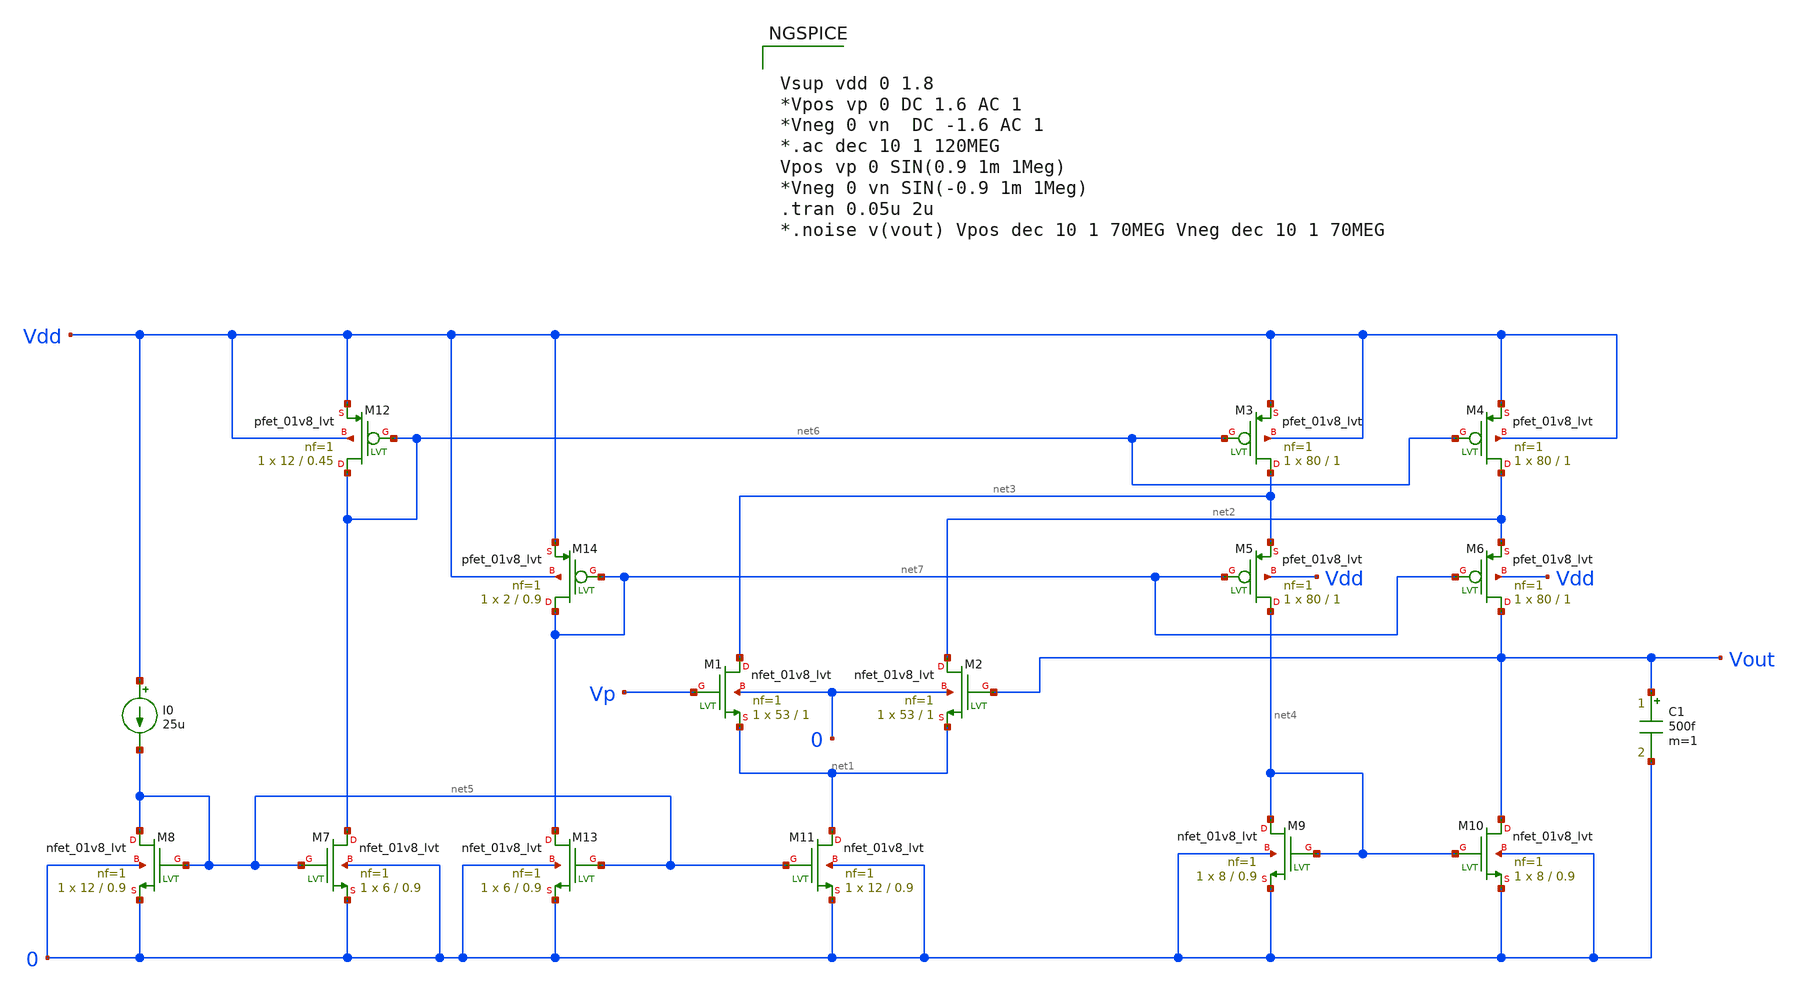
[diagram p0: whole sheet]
** sch_path: OTA/Schematic/Folded_Cascode_OTA.sch
**.subckt Folded_Cascode_OTA
XM1 net3 Vp net1 0 sky130_fd_pr__nfet_01v8_lvt L=1 W=53 nf=1 ad='int((nf+1)/2) * W/nf * 0.29' as='int((nf+2)/2) * W/nf * 0.29'
+ pd='2*int((nf+1)/2) * (W/nf + 0.29)' ps='2*int((nf+2)/2) * (W/nf + 0.29)' nrd='0.29 / W' nrs='0.29 / W'
+ sa=0 sb=0 sd=0 mult=1 m=1
XM2 net2 Vout net1 0 sky130_fd_pr__nfet_01v8_lvt L=1 W=53 nf=1 ad='int((nf+1)/2) * W/nf * 0.29' as='int((nf+2)/2) * W/nf * 0.29'
+ pd='2*int((nf+1)/2) * (W/nf + 0.29)' ps='2*int((nf+2)/2) * (W/nf + 0.29)' nrd='0.29 / W' nrs='0.29 / W'
+ sa=0 sb=0 sd=0 mult=1 m=1
XM3 net3 net6 Vdd Vdd sky130_fd_pr__pfet_01v8_lvt L=1 W=80 nf=1 ad='int((nf+1)/2) * W/nf * 0.29' as='int((nf+2)/2) * W/nf * 0.29'
+ pd='2*int((nf+1)/2) * (W/nf + 0.29)' ps='2*int((nf+2)/2) * (W/nf + 0.29)' nrd='0.29 / W' nrs='0.29 / W'
+ sa=0 sb=0 sd=0 mult=1 m=1
XM4 net2 net6 Vdd Vdd sky130_fd_pr__pfet_01v8_lvt L=1 W=80 nf=1 ad='int((nf+1)/2) * W/nf * 0.29' as='int((nf+2)/2) * W/nf * 0.29'
+ pd='2*int((nf+1)/2) * (W/nf + 0.29)' ps='2*int((nf+2)/2) * (W/nf + 0.29)' nrd='0.29 / W' nrs='0.29 / W'
+ sa=0 sb=0 sd=0 mult=1 m=1
XM5 net4 net7 net3 Vdd sky130_fd_pr__pfet_01v8_lvt L=1 W=80 nf=1 ad='int((nf+1)/2) * W/nf * 0.29' as='int((nf+2)/2) * W/nf * 0.29'
+ pd='2*int((nf+1)/2) * (W/nf + 0.29)' ps='2*int((nf+2)/2) * (W/nf + 0.29)' nrd='0.29 / W' nrs='0.29 / W'
+ sa=0 sb=0 sd=0 mult=1 m=1
XM6 Vout net7 net2 Vdd sky130_fd_pr__pfet_01v8_lvt L=1 W=80 nf=1 ad='int((nf+1)/2) * W/nf * 0.29' as='int((nf+2)/2) * W/nf * 0.29'
+ pd='2*int((nf+1)/2) * (W/nf + 0.29)' ps='2*int((nf+2)/2) * (W/nf + 0.29)' nrd='0.29 / W' nrs='0.29 / W'
+ sa=0 sb=0 sd=0 mult=1 m=1
XM9 net4 net4 0 0 sky130_fd_pr__nfet_01v8_lvt L=0.9 W=8 nf=1 ad='int((nf+1)/2) * W/nf * 0.29' as='int((nf+2)/2) * W/nf * 0.29'
+ pd='2*int((nf+1)/2) * (W/nf + 0.29)' ps='2*int((nf+2)/2) * (W/nf + 0.29)' nrd='0.29 / W' nrs='0.29 / W'
+ sa=0 sb=0 sd=0 mult=1 m=1
XM10 Vout net4 0 0 sky130_fd_pr__nfet_01v8_lvt L=0.9 W=8 nf=1 ad='int((nf+1)/2) * W/nf * 0.29' as='int((nf+2)/2) * W/nf * 0.29'
+ pd='2*int((nf+1)/2) * (W/nf + 0.29)' ps='2*int((nf+2)/2) * (W/nf + 0.29)' nrd='0.29 / W' nrs='0.29 / W'
+ sa=0 sb=0 sd=0 mult=1 m=1
XM11 net1 net5 0 0 sky130_fd_pr__nfet_01v8_lvt L=0.9 W=12 nf=1 ad='int((nf+1)/2) * W/nf * 0.29' as='int((nf+2)/2) * W/nf * 0.29'
+ pd='2*int((nf+1)/2) * (W/nf + 0.29)' ps='2*int((nf+2)/2) * (W/nf + 0.29)' nrd='0.29 / W' nrs='0.29 / W'
+ sa=0 sb=0 sd=0 mult=1 m=1
XM7 net6 net5 0 0 sky130_fd_pr__nfet_01v8_lvt L=0.9 W=6 nf=1 ad='int((nf+1)/2) * W/nf * 0.29' as='int((nf+2)/2) * W/nf * 0.29'
+ pd='2*int((nf+1)/2) * (W/nf + 0.29)' ps='2*int((nf+2)/2) * (W/nf + 0.29)' nrd='0.29 / W' nrs='0.29 / W'
+ sa=0 sb=0 sd=0 mult=1 m=1
XM8 net5 net5 0 0 sky130_fd_pr__nfet_01v8_lvt L=0.9 W=12 nf=1 ad='int((nf+1)/2) * W/nf * 0.29' as='int((nf+2)/2) * W/nf * 0.29'
+ pd='2*int((nf+1)/2) * (W/nf + 0.29)' ps='2*int((nf+2)/2) * (W/nf + 0.29)' nrd='0.29 / W' nrs='0.29 / W'
+ sa=0 sb=0 sd=0 mult=1 m=1
XM12 net6 net6 Vdd Vdd sky130_fd_pr__pfet_01v8_lvt L=0.45 W=12 nf=1 ad='int((nf+1)/2) * W/nf * 0.29'
+ as='int((nf+2)/2) * W/nf * 0.29' pd='2*int((nf+1)/2) * (W/nf + 0.29)' ps='2*int((nf+2)/2) * (W/nf + 0.29)'
+ nrd='0.29 / W' nrs='0.29 / W' sa=0 sb=0 sd=0 mult=1 m=1
XM13 net7 net5 0 0 sky130_fd_pr__nfet_01v8_lvt L=0.9 W=6 nf=1 ad='int((nf+1)/2) * W/nf * 0.29' as='int((nf+2)/2) * W/nf * 0.29'
+ pd='2*int((nf+1)/2) * (W/nf + 0.29)' ps='2*int((nf+2)/2) * (W/nf + 0.29)' nrd='0.29 / W' nrs='0.29 / W'
+ sa=0 sb=0 sd=0 mult=1 m=1
XM14 net7 net7 Vdd Vdd sky130_fd_pr__pfet_01v8_lvt L=0.9 W=2 nf=1 ad='int((nf+1)/2) * W/nf * 0.29' as='int((nf+2)/2) * W/nf * 0.29'
+ pd='2*int((nf+1)/2) * (W/nf + 0.29)' ps='2*int((nf+2)/2) * (W/nf + 0.29)' nrd='0.29 / W' nrs='0.29 / W'
+ sa=0 sb=0 sd=0 mult=1 m=1
I0 Vdd net5 25u
C1 Vout 0 500f m=1
**** begin user architecture code

.include $::SKYWATER_MODELS/cells/nfet_01v8/sky130_fd_pr__nfet_01v8__tt.corner.spice
.include $::SKYWATER_MODELS/cells/nfet_01v8_lvt/sky130_fd_pr__nfet_01v8_lvt__tt.corner.spice
.include $::SKYWATER_MODELS/cells/pfet_01v8/sky130_fd_pr__pfet_01v8__tt.corner.spice
.include $::SKYWATER_MODELS/cells/nfet_03v3_nvt/sky130_fd_pr__nfet_03v3_nvt__tt.corner.spice
.include $::SKYWATER_MODELS/cells/nfet_05v0_nvt/sky130_fd_pr__nfet_05v0_nvt__tt.corner.spice
.include $::SKYWATER_MODELS/cells/esd_nfet_01v8/sky130_fd_pr__esd_nfet_01v8__tt.corner.spice
.include $::SKYWATER_MODELS/cells/pfet_01v8_lvt/sky130_fd_pr__pfet_01v8_lvt__tt.corner.spice
.include $::SKYWATER_MODELS/cells/pfet_01v8_hvt/sky130_fd_pr__pfet_01v8_hvt__tt.corner.spice
.include $::SKYWATER_MODELS/cells/esd_pfet_g5v0d10v5/sky130_fd_pr__esd_pfet_g5v0d10v5__tt.corner.spice
.include $::SKYWATER_MODELS/cells/pfet_g5v0d10v5/sky130_fd_pr__pfet_g5v0d10v5__tt.corner.spice
.include $::SKYWATER_MODELS/cells/pfet_g5v0d16v0/sky130_fd_pr__pfet_g5v0d16v0__tt.corner.spice
.include $::SKYWATER_MODELS/cells/nfet_g5v0d10v5/sky130_fd_pr__nfet_g5v0d10v5__tt.corner.spice
.include $::SKYWATER_MODELS/cells/nfet_g5v0d16v0/sky130_fd_pr__nfet_g5v0d16v0__tt_discrete.corner.spice
.include $::SKYWATER_MODELS/cells/esd_nfet_g5v0d10v5/sky130_fd_pr__esd_nfet_g5v0d10v5__tt.corner.spice
.include $::SKYWATER_MODELS/models/corners/tt/nonfet.spice
* Mismatch parameters
.include $::SKYWATER_MODELS/cells/nfet_01v8/sky130_fd_pr__nfet_01v8__mismatch.corner.spice
.include $::SKYWATER_MODELS/cells/pfet_01v8/sky130_fd_pr__pfet_01v8__mismatch.corner.spice
.include $::SKYWATER_MODELS/cells/nfet_01v8_lvt/sky130_fd_pr__nfet_01v8_lvt__mismatch.corner.spice
.include $::SKYWATER_MODELS/cells/pfet_01v8_lvt/sky130_fd_pr__pfet_01v8_lvt__mismatch.corner.spice
.include $::SKYWATER_MODELS/cells/pfet_01v8_hvt/sky130_fd_pr__pfet_01v8_hvt__mismatch.corner.spice
.include $::SKYWATER_MODELS/cells/nfet_g5v0d10v5/sky130_fd_pr__nfet_g5v0d10v5__mismatch.corner.spice
.include $::SKYWATER_MODELS/cells/pfet_g5v0d10v5/sky130_fd_pr__pfet_g5v0d10v5__mismatch.corner.spice
.include $::SKYWATER_MODELS/cells/nfet_05v0_nvt/sky130_fd_pr__nfet_05v0_nvt__mismatch.corner.spice
.include $::SKYWATER_MODELS/cells/nfet_03v3_nvt/sky130_fd_pr__nfet_03v3_nvt__mismatch.corner.spice
* Resistor$::SKYWATER_MODELS/Capacitor
.include $::SKYWATER_MODELS/models/r+c/res_typical__cap_typical.spice
.include $::SKYWATER_MODELS/models/r+c/res_typical__cap_typical__lin.spice
* Special cells
.include $::SKYWATER_MODELS/models/corners/tt/specialized_cells.spice
* All models
.include $::SKYWATER_MODELS/models/all.spice
* Corner
.include $::SKYWATER_MODELS/models/corners/tt/rf.spice



Vsup vdd 0 1.8
*Vpos vp 0 DC 1.6 AC 1
*Vneg 0 vn  DC -1.6 AC 1
*.ac dec 10 1 120MEG
Vpos vp 0 SIN(0.9 1m 1Meg)
*Vneg 0 vn SIN(-0.9 1m 1Meg)
.tran 0.05u 2u
*.noise v(vout) Vpos dec 10 1 70MEG Vneg dec 10 1 70MEG


**** end user architecture code
**.ends
.end
